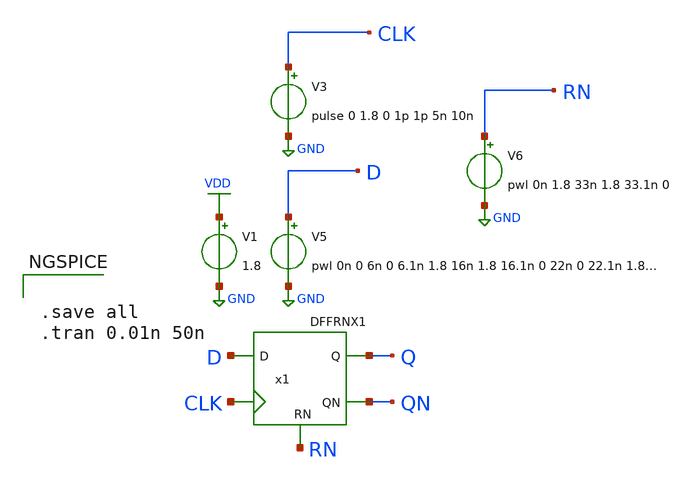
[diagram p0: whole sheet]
** sch_path: current/xschem/test_DFFRNX1.sch
**.subckt test_DFFRNX1
V1 VDD GND 1.8
V3 CLK GND pulse 0 1.8 0 1p 1p 5n 10n
x1 Q QN D CLK RN VDD GND DFFRNX1
V5 D GND pwl 0n 0 6n 0 6.1n 1.8 16n 1.8 16.1n 0 22n 0 22.1n 1.8 32n 1.8 32.1n 0
V6 RN GND pwl 0n 1.8 33n 1.8 33.1n 0
**** begin user architecture code

.lib $::SKYWATER_MODELS/sky130.lib.spice tt


**** end user architecture code
**.ends
.GLOBAL VDD
.GLOBAL GND
**** begin user architecture code


.save all
.tran 0.01n 50n


**** end user architecture code
.end
